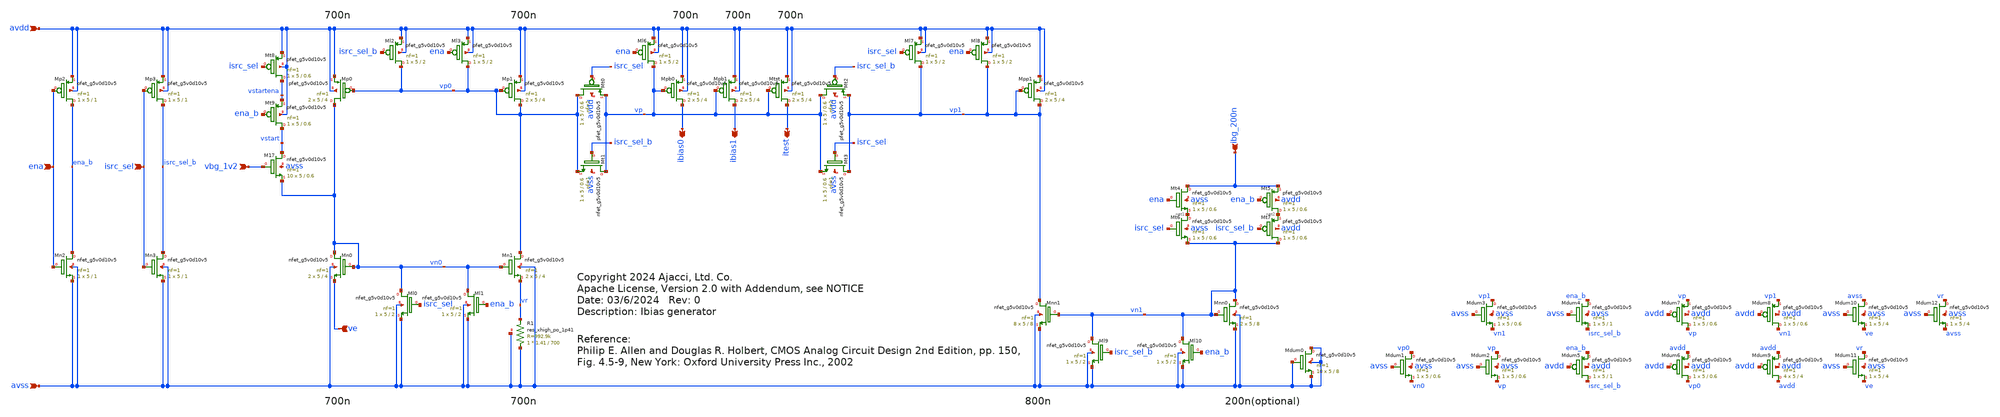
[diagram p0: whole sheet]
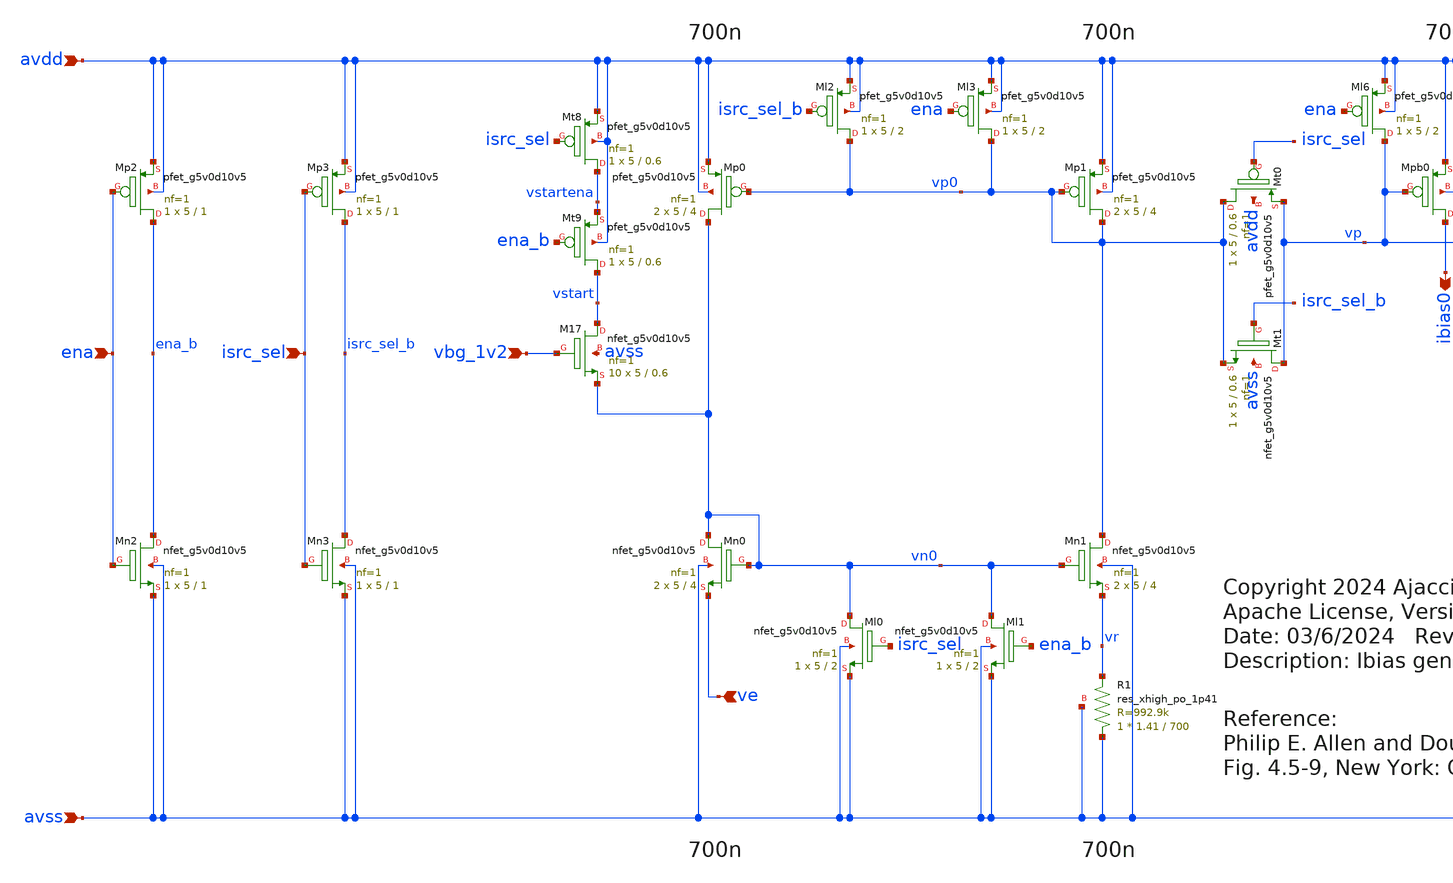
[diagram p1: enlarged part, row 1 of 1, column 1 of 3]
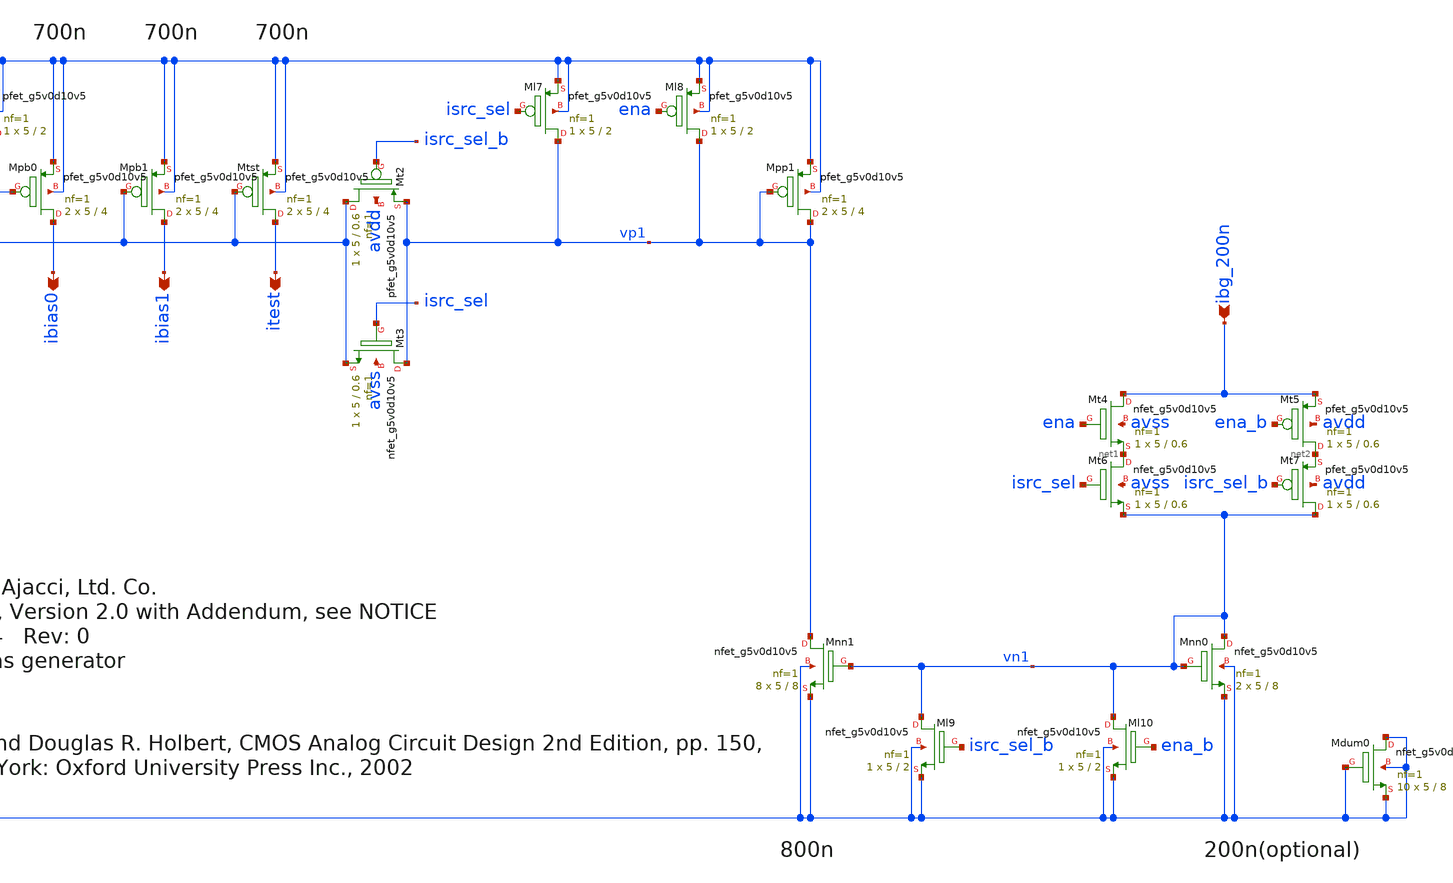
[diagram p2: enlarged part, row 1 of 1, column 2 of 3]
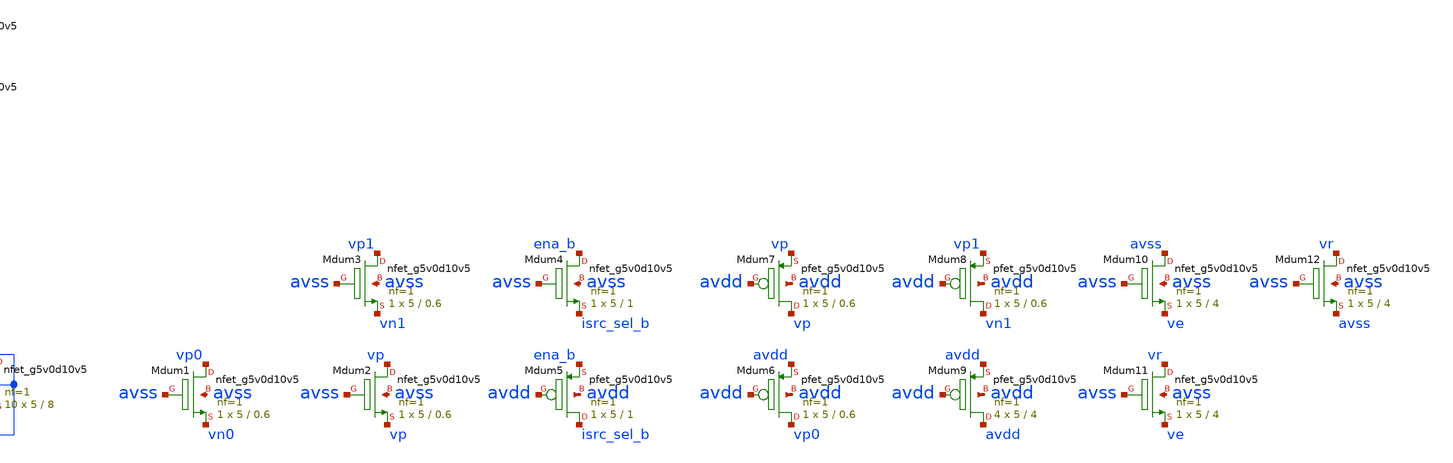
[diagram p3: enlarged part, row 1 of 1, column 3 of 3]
** sch_path: xschem/ibias_gen.sch
* Copyright 2024 Ajacci, Ltd. Co.
* Apache License, Version 2.0 with Addendum, see NOTICE
**.subckt ibias_gen vbg_1v2 ena ibias0 ibg_200n isrc_sel avdd avss itest ve ibias1
*.ipin vbg_1v2
*.ipin ena
*.opin ibias0
*.ipin ibg_200n
*.ipin isrc_sel
*.ipin avdd
*.ipin avss
*.opin itest
*.ipin ve
*.opin ibias1
XM17 vstart vbg_1v2 vn0 avss sky130_fd_pr__nfet_g5v0d10v5 L=0.6 W=5 nf=1 ad='int((nf+1)/2) * W/nf * 0.29'
+ as='int((nf+2)/2) * W/nf * 0.29' pd='2*int((nf+1)/2) * (W/nf + 0.29)' ps='2*int((nf+2)/2) * (W/nf + 0.29)'
+ nrd='0.29 / W' nrs='0.29 / W' sa=0 sb=0 sd=0 mult=10 m=10
XMt9 vstart ena_b vstartena avdd sky130_fd_pr__pfet_g5v0d10v5 L=0.6 W=5 nf=1 ad='int((nf+1)/2) * W/nf * 0.29'
+ as='int((nf+2)/2) * W/nf * 0.29' pd='2*int((nf+1)/2) * (W/nf + 0.29)' ps='2*int((nf+2)/2) * (W/nf + 0.29)'
+ nrd='0.29 / W' nrs='0.29 / W' sa=0 sb=0 sd=0 mult=1 m=1
XMn0 vn0 vn0 ve avss sky130_fd_pr__nfet_g5v0d10v5 L=4 W=5 nf=1 ad='int((nf+1)/2) * W/nf * 0.29' as='int((nf+2)/2) * W/nf * 0.29'
+ pd='2*int((nf+1)/2) * (W/nf + 0.29)' ps='2*int((nf+2)/2) * (W/nf + 0.29)' nrd='0.29 / W' nrs='0.29 / W'
+ sa=0 sb=0 sd=0 mult=2 m=2
XMp0 vn0 vp0 avdd avdd sky130_fd_pr__pfet_g5v0d10v5 L=4 W=5 nf=1 ad='int((nf+1)/2) * W/nf * 0.29' as='int((nf+2)/2) * W/nf * 0.29'
+ pd='2*int((nf+1)/2) * (W/nf + 0.29)' ps='2*int((nf+2)/2) * (W/nf + 0.29)' nrd='0.29 / W' nrs='0.29 / W'
+ sa=0 sb=0 sd=0 mult=2 m=2
XMn1 vp0 vn0 vr avss sky130_fd_pr__nfet_g5v0d10v5 L=4 W=5 nf=1 ad='int((nf+1)/2) * W/nf * 0.29' as='int((nf+2)/2) * W/nf * 0.29'
+ pd='2*int((nf+1)/2) * (W/nf + 0.29)' ps='2*int((nf+2)/2) * (W/nf + 0.29)' nrd='0.29 / W' nrs='0.29 / W'
+ sa=0 sb=0 sd=0 mult=2 m=2
XMp1 vp0 vp0 avdd avdd sky130_fd_pr__pfet_g5v0d10v5 L=4 W=5 nf=1 ad='int((nf+1)/2) * W/nf * 0.29' as='int((nf+2)/2) * W/nf * 0.29'
+ pd='2*int((nf+1)/2) * (W/nf + 0.29)' ps='2*int((nf+2)/2) * (W/nf + 0.29)' nrd='0.29 / W' nrs='0.29 / W'
+ sa=0 sb=0 sd=0 mult=2 m=2
XMpb0 ibias0 vp avdd avdd sky130_fd_pr__pfet_g5v0d10v5 L=4 W=5 nf=1 ad='int((nf+1)/2) * W/nf * 0.29'
+ as='int((nf+2)/2) * W/nf * 0.29' pd='2*int((nf+1)/2) * (W/nf + 0.29)' ps='2*int((nf+2)/2) * (W/nf + 0.29)'
+ nrd='0.29 / W' nrs='0.29 / W' sa=0 sb=0 sd=0 mult=2 m=2
XMt0 vp0 isrc_sel vp avdd sky130_fd_pr__pfet_g5v0d10v5 L=0.6 W=5 nf=1 ad='int((nf+1)/2) * W/nf * 0.29'
+ as='int((nf+2)/2) * W/nf * 0.29' pd='2*int((nf+1)/2) * (W/nf + 0.29)' ps='2*int((nf+2)/2) * (W/nf + 0.29)'
+ nrd='0.29 / W' nrs='0.29 / W' sa=0 sb=0 sd=0 mult=1 m=1
XMt1 vp isrc_sel_b vp0 avss sky130_fd_pr__nfet_g5v0d10v5 L=0.6 W=5 nf=1 ad='int((nf+1)/2) * W/nf * 0.29'
+ as='int((nf+2)/2) * W/nf * 0.29' pd='2*int((nf+1)/2) * (W/nf + 0.29)' ps='2*int((nf+2)/2) * (W/nf + 0.29)'
+ nrd='0.29 / W' nrs='0.29 / W' sa=0 sb=0 sd=0 mult=1 m=1
XMl6 vp ena avdd avdd sky130_fd_pr__pfet_g5v0d10v5 L=2 W=5 nf=1 ad='int((nf+1)/2) * W/nf * 0.29' as='int((nf+2)/2) * W/nf * 0.29'
+ pd='2*int((nf+1)/2) * (W/nf + 0.29)' ps='2*int((nf+2)/2) * (W/nf + 0.29)' nrd='0.29 / W' nrs='0.29 / W'
+ sa=0 sb=0 sd=0 mult=1 m=1
XMl3 vp0 ena avdd avdd sky130_fd_pr__pfet_g5v0d10v5 L=2 W=5 nf=1 ad='int((nf+1)/2) * W/nf * 0.29' as='int((nf+2)/2) * W/nf * 0.29'
+ pd='2*int((nf+1)/2) * (W/nf + 0.29)' ps='2*int((nf+2)/2) * (W/nf + 0.29)' nrd='0.29 / W' nrs='0.29 / W'
+ sa=0 sb=0 sd=0 mult=1 m=1
XMl1 vn0 ena_b avss avss sky130_fd_pr__nfet_g5v0d10v5 L=2 W=5 nf=1 ad='int((nf+1)/2) * W/nf * 0.29' as='int((nf+2)/2) * W/nf * 0.29'
+ pd='2*int((nf+1)/2) * (W/nf + 0.29)' ps='2*int((nf+2)/2) * (W/nf + 0.29)' nrd='0.29 / W' nrs='0.29 / W'
+ sa=0 sb=0 sd=0 mult=1 m=1
XMnn1 vp1 vn1 avss avss sky130_fd_pr__nfet_g5v0d10v5 L=8 W=5 nf=1 ad='int((nf+1)/2) * W/nf * 0.29' as='int((nf+2)/2) * W/nf * 0.29'
+ pd='2*int((nf+1)/2) * (W/nf + 0.29)' ps='2*int((nf+2)/2) * (W/nf + 0.29)' nrd='0.29 / W' nrs='0.29 / W'
+ sa=0 sb=0 sd=0 mult=8 m=8
XMnn0 vn1 vn1 avss avss sky130_fd_pr__nfet_g5v0d10v5 L=8 W=5 nf=1 ad='int((nf+1)/2) * W/nf * 0.29' as='int((nf+2)/2) * W/nf * 0.29'
+ pd='2*int((nf+1)/2) * (W/nf + 0.29)' ps='2*int((nf+2)/2) * (W/nf + 0.29)' nrd='0.29 / W' nrs='0.29 / W'
+ sa=0 sb=0 sd=0 mult=2 m=2
XMl9 vn1 isrc_sel_b avss avss sky130_fd_pr__nfet_g5v0d10v5 L=2 W=5 nf=1 ad='int((nf+1)/2) * W/nf * 0.29'
+ as='int((nf+2)/2) * W/nf * 0.29' pd='2*int((nf+1)/2) * (W/nf + 0.29)' ps='2*int((nf+2)/2) * (W/nf + 0.29)'
+ nrd='0.29 / W' nrs='0.29 / W' sa=0 sb=0 sd=0 mult=1 m=1
XMt6 net1 isrc_sel vn1 avss sky130_fd_pr__nfet_g5v0d10v5 L=0.6 W=5 nf=1 ad='int((nf+1)/2) * W/nf * 0.29'
+ as='int((nf+2)/2) * W/nf * 0.29' pd='2*int((nf+1)/2) * (W/nf + 0.29)' ps='2*int((nf+2)/2) * (W/nf + 0.29)'
+ nrd='0.29 / W' nrs='0.29 / W' sa=0 sb=0 sd=0 mult=1 m=1
XMt7 vn1 isrc_sel_b net2 avdd sky130_fd_pr__pfet_g5v0d10v5 L=0.6 W=5 nf=1 ad='int((nf+1)/2) * W/nf * 0.29'
+ as='int((nf+2)/2) * W/nf * 0.29' pd='2*int((nf+1)/2) * (W/nf + 0.29)' ps='2*int((nf+2)/2) * (W/nf + 0.29)'
+ nrd='0.29 / W' nrs='0.29 / W' sa=0 sb=0 sd=0 mult=1 m=1
XMpp1 vp1 vp1 avdd avdd sky130_fd_pr__pfet_g5v0d10v5 L=4 W=5 nf=1 ad='int((nf+1)/2) * W/nf * 0.29' as='int((nf+2)/2) * W/nf * 0.29'
+ pd='2*int((nf+1)/2) * (W/nf + 0.29)' ps='2*int((nf+2)/2) * (W/nf + 0.29)' nrd='0.29 / W' nrs='0.29 / W'
+ sa=0 sb=0 sd=0 mult=2 m=2
XMt2 vp isrc_sel_b vp1 avdd sky130_fd_pr__pfet_g5v0d10v5 L=0.6 W=5 nf=1 ad='int((nf+1)/2) * W/nf * 0.29'
+ as='int((nf+2)/2) * W/nf * 0.29' pd='2*int((nf+1)/2) * (W/nf + 0.29)' ps='2*int((nf+2)/2) * (W/nf + 0.29)'
+ nrd='0.29 / W' nrs='0.29 / W' sa=0 sb=0 sd=0 mult=1 m=1
XMt3 vp1 isrc_sel vp avss sky130_fd_pr__nfet_g5v0d10v5 L=0.6 W=5 nf=1 ad='int((nf+1)/2) * W/nf * 0.29'
+ as='int((nf+2)/2) * W/nf * 0.29' pd='2*int((nf+1)/2) * (W/nf + 0.29)' ps='2*int((nf+2)/2) * (W/nf + 0.29)'
+ nrd='0.29 / W' nrs='0.29 / W' sa=0 sb=0 sd=0 mult=1 m=1
XMt4 ibg_200n ena net1 avss sky130_fd_pr__nfet_g5v0d10v5 L=0.6 W=5 nf=1 ad='int((nf+1)/2) * W/nf * 0.29'
+ as='int((nf+2)/2) * W/nf * 0.29' pd='2*int((nf+1)/2) * (W/nf + 0.29)' ps='2*int((nf+2)/2) * (W/nf + 0.29)'
+ nrd='0.29 / W' nrs='0.29 / W' sa=0 sb=0 sd=0 mult=1 m=1
XMt5 net2 ena_b ibg_200n avdd sky130_fd_pr__pfet_g5v0d10v5 L=0.6 W=5 nf=1 ad='int((nf+1)/2) * W/nf * 0.29'
+ as='int((nf+2)/2) * W/nf * 0.29' pd='2*int((nf+1)/2) * (W/nf + 0.29)' ps='2*int((nf+2)/2) * (W/nf + 0.29)'
+ nrd='0.29 / W' nrs='0.29 / W' sa=0 sb=0 sd=0 mult=1 m=1
XMl7 vp1 isrc_sel avdd avdd sky130_fd_pr__pfet_g5v0d10v5 L=2 W=5 nf=1 ad='int((nf+1)/2) * W/nf * 0.29'
+ as='int((nf+2)/2) * W/nf * 0.29' pd='2*int((nf+1)/2) * (W/nf + 0.29)' ps='2*int((nf+2)/2) * (W/nf + 0.29)'
+ nrd='0.29 / W' nrs='0.29 / W' sa=0 sb=0 sd=0 mult=1 m=1
XMl8 vp1 ena avdd avdd sky130_fd_pr__pfet_g5v0d10v5 L=2 W=5 nf=1 ad='int((nf+1)/2) * W/nf * 0.29' as='int((nf+2)/2) * W/nf * 0.29'
+ pd='2*int((nf+1)/2) * (W/nf + 0.29)' ps='2*int((nf+2)/2) * (W/nf + 0.29)' nrd='0.29 / W' nrs='0.29 / W'
+ sa=0 sb=0 sd=0 mult=1 m=1
XMl10 vn1 ena_b avss avss sky130_fd_pr__nfet_g5v0d10v5 L=2 W=5 nf=1 ad='int((nf+1)/2) * W/nf * 0.29'
+ as='int((nf+2)/2) * W/nf * 0.29' pd='2*int((nf+1)/2) * (W/nf + 0.29)' ps='2*int((nf+2)/2) * (W/nf + 0.29)'
+ nrd='0.29 / W' nrs='0.29 / W' sa=0 sb=0 sd=0 mult=1 m=1
XMl2 vp0 isrc_sel_b avdd avdd sky130_fd_pr__pfet_g5v0d10v5 L=2 W=5 nf=1 ad='int((nf+1)/2) * W/nf * 0.29'
+ as='int((nf+2)/2) * W/nf * 0.29' pd='2*int((nf+1)/2) * (W/nf + 0.29)' ps='2*int((nf+2)/2) * (W/nf + 0.29)'
+ nrd='0.29 / W' nrs='0.29 / W' sa=0 sb=0 sd=0 mult=1 m=1
XMl0 vn0 isrc_sel avss avss sky130_fd_pr__nfet_g5v0d10v5 L=2 W=5 nf=1 ad='int((nf+1)/2) * W/nf * 0.29'
+ as='int((nf+2)/2) * W/nf * 0.29' pd='2*int((nf+1)/2) * (W/nf + 0.29)' ps='2*int((nf+2)/2) * (W/nf + 0.29)'
+ nrd='0.29 / W' nrs='0.29 / W' sa=0 sb=0 sd=0 mult=1 m=1
XMt8 vstartena isrc_sel avdd avdd sky130_fd_pr__pfet_g5v0d10v5 L=0.6 W=5 nf=1 ad='int((nf+1)/2) * W/nf * 0.29'
+ as='int((nf+2)/2) * W/nf * 0.29' pd='2*int((nf+1)/2) * (W/nf + 0.29)' ps='2*int((nf+2)/2) * (W/nf + 0.29)'
+ nrd='0.29 / W' nrs='0.29 / W' sa=0 sb=0 sd=0 mult=1 m=1
XMn2 ena_b ena avss avss sky130_fd_pr__nfet_g5v0d10v5 L=1 W=5 nf=1 ad='int((nf+1)/2) * W/nf * 0.29' as='int((nf+2)/2) * W/nf * 0.29'
+ pd='2*int((nf+1)/2) * (W/nf + 0.29)' ps='2*int((nf+2)/2) * (W/nf + 0.29)' nrd='0.29 / W' nrs='0.29 / W'
+ sa=0 sb=0 sd=0 mult=1 m=1
XMp2 ena_b ena avdd avdd sky130_fd_pr__pfet_g5v0d10v5 L=1 W=5 nf=1 ad='int((nf+1)/2) * W/nf * 0.29' as='int((nf+2)/2) * W/nf * 0.29'
+ pd='2*int((nf+1)/2) * (W/nf + 0.29)' ps='2*int((nf+2)/2) * (W/nf + 0.29)' nrd='0.29 / W' nrs='0.29 / W'
+ sa=0 sb=0 sd=0 mult=1 m=1
XMn3 isrc_sel_b isrc_sel avss avss sky130_fd_pr__nfet_g5v0d10v5 L=1 W=5 nf=1 ad='int((nf+1)/2) * W/nf * 0.29'
+ as='int((nf+2)/2) * W/nf * 0.29' pd='2*int((nf+1)/2) * (W/nf + 0.29)' ps='2*int((nf+2)/2) * (W/nf + 0.29)'
+ nrd='0.29 / W' nrs='0.29 / W' sa=0 sb=0 sd=0 mult=1 m=1
XMp3 isrc_sel_b isrc_sel avdd avdd sky130_fd_pr__pfet_g5v0d10v5 L=1 W=5 nf=1 ad='int((nf+1)/2) * W/nf * 0.29'
+ as='int((nf+2)/2) * W/nf * 0.29' pd='2*int((nf+1)/2) * (W/nf + 0.29)' ps='2*int((nf+2)/2) * (W/nf + 0.29)'
+ nrd='0.29 / W' nrs='0.29 / W' sa=0 sb=0 sd=0 mult=1 m=1
XMtst itest vp avdd avdd sky130_fd_pr__pfet_g5v0d10v5 L=4 W=5 nf=1 ad='int((nf+1)/2) * W/nf * 0.29' as='int((nf+2)/2) * W/nf * 0.29'
+ pd='2*int((nf+1)/2) * (W/nf + 0.29)' ps='2*int((nf+2)/2) * (W/nf + 0.29)' nrd='0.29 / W' nrs='0.29 / W'
+ sa=0 sb=0 sd=0 mult=2 m=2
XR1 avss vr avss sky130_fd_pr__res_xhigh_po_1p41 L=700 mult=1 m=1
XMdum0 avss avss avss avss sky130_fd_pr__nfet_g5v0d10v5 L=8 W=5 nf=1 ad='int((nf+1)/2) * W/nf * 0.29'
+ as='int((nf+2)/2) * W/nf * 0.29' pd='2*int((nf+1)/2) * (W/nf + 0.29)' ps='2*int((nf+2)/2) * (W/nf + 0.29)'
+ nrd='0.29 / W' nrs='0.29 / W' sa=0 sb=0 sd=0 mult=10 m=10
XMdum1 vp0 avss vn0 avss sky130_fd_pr__nfet_g5v0d10v5 L=0.6 W=5 nf=1 ad='int((nf+1)/2) * W/nf * 0.29'
+ as='int((nf+2)/2) * W/nf * 0.29' pd='2*int((nf+1)/2) * (W/nf + 0.29)' ps='2*int((nf+2)/2) * (W/nf + 0.29)'
+ nrd='0.29 / W' nrs='0.29 / W' sa=0 sb=0 sd=0 mult=1 m=1
XMdum2 vp avss vp avss sky130_fd_pr__nfet_g5v0d10v5 L=0.6 W=5 nf=1 ad='int((nf+1)/2) * W/nf * 0.29' as='int((nf+2)/2) * W/nf * 0.29'
+ pd='2*int((nf+1)/2) * (W/nf + 0.29)' ps='2*int((nf+2)/2) * (W/nf + 0.29)' nrd='0.29 / W' nrs='0.29 / W'
+ sa=0 sb=0 sd=0 mult=1 m=1
XMdum3 vp1 avss vn1 avss sky130_fd_pr__nfet_g5v0d10v5 L=0.6 W=5 nf=1 ad='int((nf+1)/2) * W/nf * 0.29'
+ as='int((nf+2)/2) * W/nf * 0.29' pd='2*int((nf+1)/2) * (W/nf + 0.29)' ps='2*int((nf+2)/2) * (W/nf + 0.29)'
+ nrd='0.29 / W' nrs='0.29 / W' sa=0 sb=0 sd=0 mult=1 m=1
XMdum4 ena_b avss isrc_sel_b avss sky130_fd_pr__nfet_g5v0d10v5 L=1 W=5 nf=1 ad='int((nf+1)/2) * W/nf * 0.29'
+ as='int((nf+2)/2) * W/nf * 0.29' pd='2*int((nf+1)/2) * (W/nf + 0.29)' ps='2*int((nf+2)/2) * (W/nf + 0.29)'
+ nrd='0.29 / W' nrs='0.29 / W' sa=0 sb=0 sd=0 mult=1 m=1
XMdum5 isrc_sel_b avdd ena_b avdd sky130_fd_pr__pfet_g5v0d10v5 L=1 W=5 nf=1 ad='int((nf+1)/2) * W/nf * 0.29'
+ as='int((nf+2)/2) * W/nf * 0.29' pd='2*int((nf+1)/2) * (W/nf + 0.29)' ps='2*int((nf+2)/2) * (W/nf + 0.29)'
+ nrd='0.29 / W' nrs='0.29 / W' sa=0 sb=0 sd=0 mult=1 m=1
XMdum6 vp0 avdd avdd avdd sky130_fd_pr__pfet_g5v0d10v5 L=0.6 W=5 nf=1 ad='int((nf+1)/2) * W/nf * 0.29'
+ as='int((nf+2)/2) * W/nf * 0.29' pd='2*int((nf+1)/2) * (W/nf + 0.29)' ps='2*int((nf+2)/2) * (W/nf + 0.29)'
+ nrd='0.29 / W' nrs='0.29 / W' sa=0 sb=0 sd=0 mult=1 m=1
XMdum7 vp avdd vp avdd sky130_fd_pr__pfet_g5v0d10v5 L=0.6 W=5 nf=1 ad='int((nf+1)/2) * W/nf * 0.29' as='int((nf+2)/2) * W/nf * 0.29'
+ pd='2*int((nf+1)/2) * (W/nf + 0.29)' ps='2*int((nf+2)/2) * (W/nf + 0.29)' nrd='0.29 / W' nrs='0.29 / W'
+ sa=0 sb=0 sd=0 mult=1 m=1
XMdum8 vn1 avdd vp1 avdd sky130_fd_pr__pfet_g5v0d10v5 L=0.6 W=5 nf=1 ad='int((nf+1)/2) * W/nf * 0.29'
+ as='int((nf+2)/2) * W/nf * 0.29' pd='2*int((nf+1)/2) * (W/nf + 0.29)' ps='2*int((nf+2)/2) * (W/nf + 0.29)'
+ nrd='0.29 / W' nrs='0.29 / W' sa=0 sb=0 sd=0 mult=1 m=1
XMdum9 avdd avdd avdd avdd sky130_fd_pr__pfet_g5v0d10v5 L=4 W=5 nf=1 ad='int((nf+1)/2) * W/nf * 0.29'
+ as='int((nf+2)/2) * W/nf * 0.29' pd='2*int((nf+1)/2) * (W/nf + 0.29)' ps='2*int((nf+2)/2) * (W/nf + 0.29)'
+ nrd='0.29 / W' nrs='0.29 / W' sa=0 sb=0 sd=0 mult=4 m=4
XMdum10 avss avss ve avss sky130_fd_pr__nfet_g5v0d10v5 L=4 W=5 nf=1 ad='int((nf+1)/2) * W/nf * 0.29'
+ as='int((nf+2)/2) * W/nf * 0.29' pd='2*int((nf+1)/2) * (W/nf + 0.29)' ps='2*int((nf+2)/2) * (W/nf + 0.29)'
+ nrd='0.29 / W' nrs='0.29 / W' sa=0 sb=0 sd=0 mult=1 m=1
XMdum11 vr avss ve avss sky130_fd_pr__nfet_g5v0d10v5 L=4 W=5 nf=1 ad='int((nf+1)/2) * W/nf * 0.29' as='int((nf+2)/2) * W/nf * 0.29'
+ pd='2*int((nf+1)/2) * (W/nf + 0.29)' ps='2*int((nf+2)/2) * (W/nf + 0.29)' nrd='0.29 / W' nrs='0.29 / W'
+ sa=0 sb=0 sd=0 mult=1 m=1
XMdum12 vr avss avss avss sky130_fd_pr__nfet_g5v0d10v5 L=4 W=5 nf=1 ad='int((nf+1)/2) * W/nf * 0.29'
+ as='int((nf+2)/2) * W/nf * 0.29' pd='2*int((nf+1)/2) * (W/nf + 0.29)' ps='2*int((nf+2)/2) * (W/nf + 0.29)'
+ nrd='0.29 / W' nrs='0.29 / W' sa=0 sb=0 sd=0 mult=1 m=1
XMpb1 ibias1 vp avdd avdd sky130_fd_pr__pfet_g5v0d10v5 L=4 W=5 nf=1 ad='int((nf+1)/2) * W/nf * 0.29'
+ as='int((nf+2)/2) * W/nf * 0.29' pd='2*int((nf+1)/2) * (W/nf + 0.29)' ps='2*int((nf+2)/2) * (W/nf + 0.29)'
+ nrd='0.29 / W' nrs='0.29 / W' sa=0 sb=0 sd=0 mult=2 m=2
**.ends
.end
